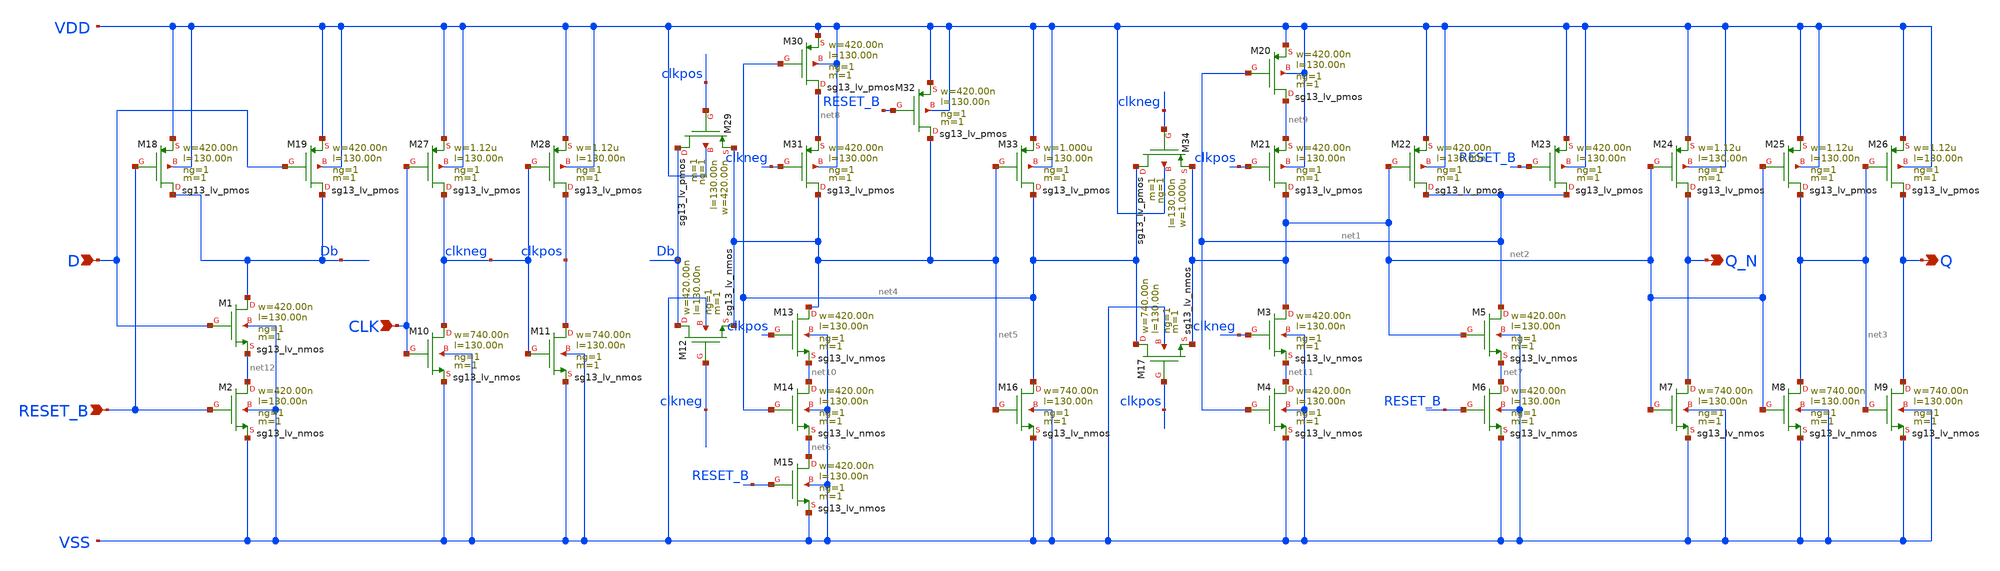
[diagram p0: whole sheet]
** sch_path: ihp-sg13g2/libs.ref/sg13g2_stdcell/sch/xschem/sg13g2_dfrbp_1.sch
**.subckt sg13g2_dfrbp_1 D RESET_B CLK Q Q_N
*.ipin D
*.ipin RESET_B
*.ipin CLK
*.opin Q
*.opin Q_N
XM1 Db D net12 VSS sg13_lv_nmos w=420.00n l=130.00n ng=1 m=1 mm_ok=1
XM2 net12 RESET_B VSS VSS sg13_lv_nmos w=420.00n l=130.00n ng=1 m=1 mm_ok=1
XM3 net2 clkneg net11 VSS sg13_lv_nmos w=420.00n l=130.00n ng=1 m=1 mm_ok=1
XM4 net11 net1 VSS VSS sg13_lv_nmos w=420.00n l=130.00n ng=1 m=1 mm_ok=1
XM5 net1 net2 net7 VSS sg13_lv_nmos w=420.00n l=130.00n ng=1 m=1 mm_ok=1
XM6 net7 RESET_B VSS VSS sg13_lv_nmos w=420.00n l=130.00n ng=1 m=1 mm_ok=1
XM7 Q_N net2 VSS VSS sg13_lv_nmos w=740.00n l=130.00n ng=1 m=1 mm_ok=1
XM8 net3 net2 VSS VSS sg13_lv_nmos w=740.00n l=130.00n ng=1 m=1 mm_ok=1
XM9 Q net3 VSS VSS sg13_lv_nmos w=740.00n l=130.00n ng=1 m=1 mm_ok=1
XM10 clkneg CLK VSS VSS sg13_lv_nmos w=740.00n l=130.00n ng=1 m=1 mm_ok=1
XM11 clkpos clkneg VSS VSS sg13_lv_nmos w=740.00n l=130.00n ng=1 m=1 mm_ok=1
XM12 Db clkneg net5 VSS sg13_lv_nmos w=420.00n l=130.00n ng=1 m=1 mm_ok=1
XM13 net5 clkpos net10 VSS sg13_lv_nmos w=420.00n l=130.00n ng=1 m=1 mm_ok=1
XM14 net10 net4 net6 VSS sg13_lv_nmos w=420.00n l=130.00n ng=1 m=1 mm_ok=1
XM15 net6 RESET_B VSS VSS sg13_lv_nmos w=420.00n l=130.00n ng=1 m=1 mm_ok=1
XM16 net4 net5 VSS VSS sg13_lv_nmos w=740.00n l=130.00n ng=1 m=1 mm_ok=1
XM17 net4 clkpos net2 VSS sg13_lv_nmos w=740.00n l=130.00n ng=1 m=1 mm_ok=1
XM18 Db RESET_B VDD VDD sg13_lv_pmos w=420.00n l=130.00n ng=1 m=1 mm_ok=1
XM19 Db D VDD VDD sg13_lv_pmos w=420.00n l=130.00n ng=1 m=1 mm_ok=1
XM20 net9 net1 VDD VDD sg13_lv_pmos w=420.00n l=130.00n ng=1 m=1 mm_ok=1
XM21 net2 clkpos net9 VDD sg13_lv_pmos w=420.00n l=130.00n ng=1 m=1 mm_ok=1
XM22 net1 net2 VDD VDD sg13_lv_pmos w=420.00n l=130.00n ng=1 m=1 mm_ok=1
XM23 net1 RESET_B VDD VDD sg13_lv_pmos w=420.00n l=130.00n ng=1 m=1 mm_ok=1
XM24 Q_N net2 VDD VDD sg13_lv_pmos w=1.12u l=130.00n ng=1 m=1 mm_ok=1
XM25 net3 net2 VDD VDD sg13_lv_pmos w=1.12u l=130.00n ng=1 m=1 mm_ok=1
XM26 Q net3 VDD VDD sg13_lv_pmos w=1.12u l=130.00n ng=1 m=1 mm_ok=1
XM27 clkneg CLK VDD VDD sg13_lv_pmos w=1.12u l=130.00n ng=1 m=1 mm_ok=1
XM28 clkpos clkneg VDD VDD sg13_lv_pmos w=1.12u l=130.00n ng=1 m=1 mm_ok=1
XM29 Db clkpos net5 VDD sg13_lv_pmos w=420.00n l=130.00n ng=1 m=1 mm_ok=1
XM30 net8 net4 VDD VDD sg13_lv_pmos w=420.00n l=130.00n ng=1 m=1 mm_ok=1
XM31 net5 clkneg net8 VDD sg13_lv_pmos w=420.00n l=130.00n ng=1 m=1 mm_ok=1
XM32 net5 RESET_B VDD VDD sg13_lv_pmos w=420.00n l=130.00n ng=1 m=1 mm_ok=1
XM33 net4 net5 VDD VDD sg13_lv_pmos w=1.000u l=130.00n ng=1 m=1 mm_ok=1
XM34 net4 clkneg net2 VDD sg13_lv_pmos w=1.000u l=130.00n ng=1 m=1 mm_ok=1
**.ends
.end
